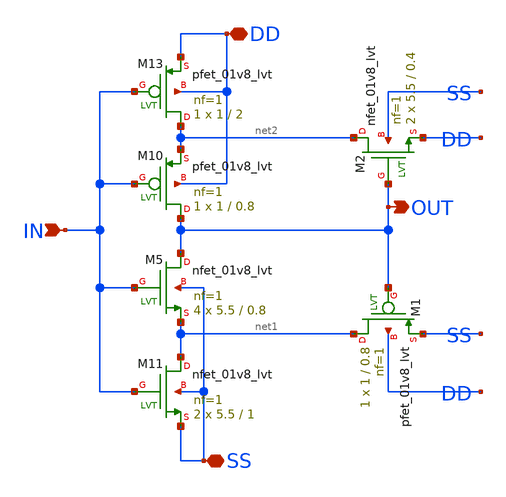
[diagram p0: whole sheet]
** sch_path: xschem/mdls_inv.sch
**.subckt mdls_inv IN DD SS OUT
*.ipin IN
*.iopin DD
*.iopin SS
*.opin OUT
XM5 OUT IN net1 SS sky130_fd_pr__nfet_01v8_lvt L=0.8 W=5.5 nf=1 ad='int((nf+1)/2) * W/nf * 0.29' as='int((nf+2)/2) * W/nf * 0.29'
+ pd='2*int((nf+1)/2) * (W/nf + 0.29)' ps='2*int((nf+2)/2) * (W/nf + 0.29)' nrd='0.29 / W' nrs='0.29 / W'
+ sa=0 sb=0 sd=0 mult=4 m=4
XM10 OUT IN net2 DD sky130_fd_pr__pfet_01v8_lvt L=0.8 W=1 nf=1 ad='int((nf+1)/2) * W/nf * 0.29' as='int((nf+2)/2) * W/nf * 0.29'
+ pd='2*int((nf+1)/2) * (W/nf + 0.29)' ps='2*int((nf+2)/2) * (W/nf + 0.29)' nrd='0.29 / W' nrs='0.29 / W'
+ sa=0 sb=0 sd=0 mult=1 m=1
XM11 net1 IN SS SS sky130_fd_pr__nfet_01v8_lvt L=1 W=5.5 nf=1 ad='int((nf+1)/2) * W/nf * 0.29' as='int((nf+2)/2) * W/nf * 0.29'
+ pd='2*int((nf+1)/2) * (W/nf + 0.29)' ps='2*int((nf+2)/2) * (W/nf + 0.29)' nrd='0.29 / W' nrs='0.29 / W'
+ sa=0 sb=0 sd=0 mult=2 m=2
XM13 net2 IN DD DD sky130_fd_pr__pfet_01v8_lvt L=2 W=1 nf=1 ad='int((nf+1)/2) * W/nf * 0.29' as='int((nf+2)/2) * W/nf * 0.29'
+ pd='2*int((nf+1)/2) * (W/nf + 0.29)' ps='2*int((nf+2)/2) * (W/nf + 0.29)' nrd='0.29 / W' nrs='0.29 / W'
+ sa=0 sb=0 sd=0 mult=1 m=1
XM1 net1 OUT SS DD sky130_fd_pr__pfet_01v8_lvt L=0.8 W=1 nf=1 ad='int((nf+1)/2) * W/nf * 0.29' as='int((nf+2)/2) * W/nf * 0.29'
+ pd='2*int((nf+1)/2) * (W/nf + 0.29)' ps='2*int((nf+2)/2) * (W/nf + 0.29)' nrd='0.29 / W' nrs='0.29 / W'
+ sa=0 sb=0 sd=0 mult=1 m=1
XM2 net2 OUT DD SS sky130_fd_pr__nfet_01v8_lvt L=0.4 W=5.5 nf=1 ad='int((nf+1)/2) * W/nf * 0.29' as='int((nf+2)/2) * W/nf * 0.29'
+ pd='2*int((nf+1)/2) * (W/nf + 0.29)' ps='2*int((nf+2)/2) * (W/nf + 0.29)' nrd='0.29 / W' nrs='0.29 / W'
+ sa=0 sb=0 sd=0 mult=2 m=2
**.ends
.end
